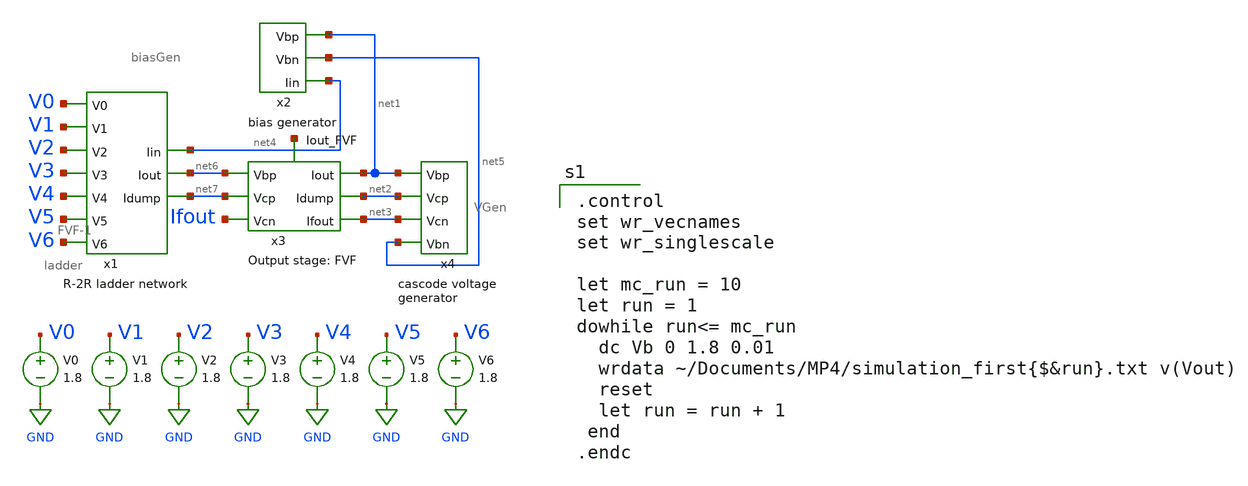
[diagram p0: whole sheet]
** sch_path: xschem/MP4-simulation-1.sch
**.subckt MP4-simulation-1
V1 V1 GND 1.8
V2 V2 GND 1.8
V3 V3 GND 1.8
V4 V4 GND 1.8
V5 V5 GND 1.8
V6 V6 GND 1.8
V0 V0 GND 1.8
x1 net4 net7 net6 V0 V1 V2 V3 V4 V5 V6 ladder
x2 net1 net4 net5 biasGen
x3 net6 net7 net1 Ifout net3 net2 net8 FVF-1
x4 net1 net3 net2 net5 VGen
**** begin user architecture code

.option wnflag=1
.param MC_SWITCH=0.0
.lib ~/skywater/skywater-pdk/libraries/sky130_fd_pr_ngspice/latest/models/sky130.lib.spice tt


.control
set wr_vecnames
set wr_singlescale

let mc_run = 10
let run = 1
dowhile run<= mc_run
  dc Vb 0 1.8 0.01
  wrdata ~/Documents/MP4/simulation_first{$&run}.txt v(Vout)
  reset
  let run = run + 1
 end
.endc

**** end user architecture code
**.ends

* expanding   symbol:  /home/madvlsi/DAC-VLSI/xschem/ladder.sym # of pins=10
** sym_path: /home/madvlsi/DAC-VLSI/xschem/ladder.sym
** sch_path: /home/madvlsi/DAC-VLSI/xschem/ladder.sch
.subckt ladder Iin Idump Iout V0 V1 V2 V3 V4 V5 V6
*.ipin Iin
*.ipin V0
*.ipin V1
*.ipin V2
*.ipin V3
*.ipin V4
*.ipin V5
*.ipin V6
*.opin Idump
*.opin Iout
XM1 Iin VDD net1 GND sky130_fd_pr__nfet_01v8 L=0.15 W=1 nf=1 ad='int((nf+1)/2) * W/nf * 0.29' as='int((nf+2)/2) * W/nf * 0.29'
+ pd='2*int((nf+1)/2) * (W/nf + 0.29)' ps='2*int((nf+2)/2) * (W/nf + 0.29)' nrd='0.29 / W' nrs='0.29 / W'
+ sa=0 sb=0 sd=0 mult=1 m=1
XM3 Iin VDD net3 GND sky130_fd_pr__nfet_01v8 L=0.15 W=1 nf=1 ad='int((nf+1)/2) * W/nf * 0.29' as='int((nf+2)/2) * W/nf * 0.29'
+ pd='2*int((nf+1)/2) * (W/nf + 0.29)' ps='2*int((nf+2)/2) * (W/nf + 0.29)' nrd='0.29 / W' nrs='0.29 / W'
+ sa=0 sb=0 sd=0 mult=1 m=1
XM5 net3 VDD net4 GND sky130_fd_pr__nfet_01v8 L=0.15 W=1 nf=1 ad='int((nf+1)/2) * W/nf * 0.29' as='int((nf+2)/2) * W/nf * 0.29'
+ pd='2*int((nf+1)/2) * (W/nf + 0.29)' ps='2*int((nf+2)/2) * (W/nf + 0.29)' nrd='0.29 / W' nrs='0.29 / W'
+ sa=0 sb=0 sd=0 mult=1 m=1
XM7 net3 VDD net6 GND sky130_fd_pr__nfet_01v8 L=0.15 W=1 nf=1 ad='int((nf+1)/2) * W/nf * 0.29' as='int((nf+2)/2) * W/nf * 0.29'
+ pd='2*int((nf+1)/2) * (W/nf + 0.29)' ps='2*int((nf+2)/2) * (W/nf + 0.29)' nrd='0.29 / W' nrs='0.29 / W'
+ sa=0 sb=0 sd=0 mult=1 m=1
XM6 net4 V1 net2 GND sky130_fd_pr__nfet_01v8 L=0.15 W=1 nf=1 ad='int((nf+1)/2) * W/nf * 0.29' as='int((nf+2)/2) * W/nf * 0.29'
+ pd='2*int((nf+1)/2) * (W/nf + 0.29)' ps='2*int((nf+2)/2) * (W/nf + 0.29)' nrd='0.29 / W' nrs='0.29 / W'
+ sa=0 sb=0 sd=0 mult=1 m=1
XM8 net4 net18 net5 GND sky130_fd_pr__nfet_01v8 L=0.15 W=1 nf=1 ad='int((nf+1)/2) * W/nf * 0.29' as='int((nf+2)/2) * W/nf * 0.29'
+ pd='2*int((nf+1)/2) * (W/nf + 0.29)' ps='2*int((nf+2)/2) * (W/nf + 0.29)' nrd='0.29 / W' nrs='0.29 / W'
+ sa=0 sb=0 sd=0 mult=1 m=1
XM2 net1 V0 net2 GND sky130_fd_pr__nfet_01v8 L=0.15 W=1 nf=1 ad='int((nf+1)/2) * W/nf * 0.29' as='int((nf+2)/2) * W/nf * 0.29'
+ pd='2*int((nf+1)/2) * (W/nf + 0.29)' ps='2*int((nf+2)/2) * (W/nf + 0.29)' nrd='0.29 / W' nrs='0.29 / W'
+ sa=0 sb=0 sd=0 mult=1 m=1
XM4 net1 net17 net5 GND sky130_fd_pr__nfet_01v8 L=0.15 W=1 nf=1 ad='int((nf+1)/2) * W/nf * 0.29' as='int((nf+2)/2) * W/nf * 0.29'
+ pd='2*int((nf+1)/2) * (W/nf + 0.29)' ps='2*int((nf+2)/2) * (W/nf + 0.29)' nrd='0.29 / W' nrs='0.29 / W'
+ sa=0 sb=0 sd=0 mult=1 m=1
XM9 net6 VDD net7 GND sky130_fd_pr__nfet_01v8 L=0.15 W=1 nf=1 ad='int((nf+1)/2) * W/nf * 0.29' as='int((nf+2)/2) * W/nf * 0.29'
+ pd='2*int((nf+1)/2) * (W/nf + 0.29)' ps='2*int((nf+2)/2) * (W/nf + 0.29)' nrd='0.29 / W' nrs='0.29 / W'
+ sa=0 sb=0 sd=0 mult=1 m=1
XM11 net6 VDD net8 GND sky130_fd_pr__nfet_01v8 L=0.15 W=1 nf=1 ad='int((nf+1)/2) * W/nf * 0.29' as='int((nf+2)/2) * W/nf * 0.29'
+ pd='2*int((nf+1)/2) * (W/nf + 0.29)' ps='2*int((nf+2)/2) * (W/nf + 0.29)' nrd='0.29 / W' nrs='0.29 / W'
+ sa=0 sb=0 sd=0 mult=1 m=1
XM10 net7 V2 net2 GND sky130_fd_pr__nfet_01v8 L=0.15 W=1 nf=1 ad='int((nf+1)/2) * W/nf * 0.29' as='int((nf+2)/2) * W/nf * 0.29'
+ pd='2*int((nf+1)/2) * (W/nf + 0.29)' ps='2*int((nf+2)/2) * (W/nf + 0.29)' nrd='0.29 / W' nrs='0.29 / W'
+ sa=0 sb=0 sd=0 mult=1 m=1
XM12 net7 net19 net5 GND sky130_fd_pr__nfet_01v8 L=0.15 W=1 nf=1 ad='int((nf+1)/2) * W/nf * 0.29' as='int((nf+2)/2) * W/nf * 0.29'
+ pd='2*int((nf+1)/2) * (W/nf + 0.29)' ps='2*int((nf+2)/2) * (W/nf + 0.29)' nrd='0.29 / W' nrs='0.29 / W'
+ sa=0 sb=0 sd=0 mult=1 m=1
XM13 net8 VDD net9 GND sky130_fd_pr__nfet_01v8 L=0.15 W=1 nf=1 ad='int((nf+1)/2) * W/nf * 0.29' as='int((nf+2)/2) * W/nf * 0.29'
+ pd='2*int((nf+1)/2) * (W/nf + 0.29)' ps='2*int((nf+2)/2) * (W/nf + 0.29)' nrd='0.29 / W' nrs='0.29 / W'
+ sa=0 sb=0 sd=0 mult=1 m=1
XM15 net8 VDD net10 GND sky130_fd_pr__nfet_01v8 L=0.15 W=1 nf=1 ad='int((nf+1)/2) * W/nf * 0.29' as='int((nf+2)/2) * W/nf * 0.29'
+ pd='2*int((nf+1)/2) * (W/nf + 0.29)' ps='2*int((nf+2)/2) * (W/nf + 0.29)' nrd='0.29 / W' nrs='0.29 / W'
+ sa=0 sb=0 sd=0 mult=1 m=1
XM14 net9 V3 net2 GND sky130_fd_pr__nfet_01v8 L=0.15 W=1 nf=1 ad='int((nf+1)/2) * W/nf * 0.29' as='int((nf+2)/2) * W/nf * 0.29'
+ pd='2*int((nf+1)/2) * (W/nf + 0.29)' ps='2*int((nf+2)/2) * (W/nf + 0.29)' nrd='0.29 / W' nrs='0.29 / W'
+ sa=0 sb=0 sd=0 mult=1 m=1
XM16 net9 net20 net5 GND sky130_fd_pr__nfet_01v8 L=0.15 W=1 nf=1 ad='int((nf+1)/2) * W/nf * 0.29' as='int((nf+2)/2) * W/nf * 0.29'
+ pd='2*int((nf+1)/2) * (W/nf + 0.29)' ps='2*int((nf+2)/2) * (W/nf + 0.29)' nrd='0.29 / W' nrs='0.29 / W'
+ sa=0 sb=0 sd=0 mult=1 m=1
XM17 net10 VDD net11 GND sky130_fd_pr__nfet_01v8 L=0.15 W=1 nf=1 ad='int((nf+1)/2) * W/nf * 0.29' as='int((nf+2)/2) * W/nf * 0.29'
+ pd='2*int((nf+1)/2) * (W/nf + 0.29)' ps='2*int((nf+2)/2) * (W/nf + 0.29)' nrd='0.29 / W' nrs='0.29 / W'
+ sa=0 sb=0 sd=0 mult=1 m=1
XM19 net10 VDD net12 GND sky130_fd_pr__nfet_01v8 L=0.15 W=1 nf=1 ad='int((nf+1)/2) * W/nf * 0.29' as='int((nf+2)/2) * W/nf * 0.29'
+ pd='2*int((nf+1)/2) * (W/nf + 0.29)' ps='2*int((nf+2)/2) * (W/nf + 0.29)' nrd='0.29 / W' nrs='0.29 / W'
+ sa=0 sb=0 sd=0 mult=1 m=1
XM18 net11 V4 net2 GND sky130_fd_pr__nfet_01v8 L=0.15 W=1 nf=1 ad='int((nf+1)/2) * W/nf * 0.29' as='int((nf+2)/2) * W/nf * 0.29'
+ pd='2*int((nf+1)/2) * (W/nf + 0.29)' ps='2*int((nf+2)/2) * (W/nf + 0.29)' nrd='0.29 / W' nrs='0.29 / W'
+ sa=0 sb=0 sd=0 mult=1 m=1
XM20 net11 net21 net5 GND sky130_fd_pr__nfet_01v8 L=0.15 W=1 nf=1 ad='int((nf+1)/2) * W/nf * 0.29' as='int((nf+2)/2) * W/nf * 0.29'
+ pd='2*int((nf+1)/2) * (W/nf + 0.29)' ps='2*int((nf+2)/2) * (W/nf + 0.29)' nrd='0.29 / W' nrs='0.29 / W'
+ sa=0 sb=0 sd=0 mult=1 m=1
XM21 net12 VDD net13 GND sky130_fd_pr__nfet_01v8 L=0.15 W=1 nf=1 ad='int((nf+1)/2) * W/nf * 0.29' as='int((nf+2)/2) * W/nf * 0.29'
+ pd='2*int((nf+1)/2) * (W/nf + 0.29)' ps='2*int((nf+2)/2) * (W/nf + 0.29)' nrd='0.29 / W' nrs='0.29 / W'
+ sa=0 sb=0 sd=0 mult=1 m=1
XM23 net12 VDD net14 GND sky130_fd_pr__nfet_01v8 L=0.15 W=1 nf=1 ad='int((nf+1)/2) * W/nf * 0.29' as='int((nf+2)/2) * W/nf * 0.29'
+ pd='2*int((nf+1)/2) * (W/nf + 0.29)' ps='2*int((nf+2)/2) * (W/nf + 0.29)' nrd='0.29 / W' nrs='0.29 / W'
+ sa=0 sb=0 sd=0 mult=1 m=1
XM22 net13 V5 net2 GND sky130_fd_pr__nfet_01v8 L=0.15 W=1 nf=1 ad='int((nf+1)/2) * W/nf * 0.29' as='int((nf+2)/2) * W/nf * 0.29'
+ pd='2*int((nf+1)/2) * (W/nf + 0.29)' ps='2*int((nf+2)/2) * (W/nf + 0.29)' nrd='0.29 / W' nrs='0.29 / W'
+ sa=0 sb=0 sd=0 mult=1 m=1
XM24 net13 net22 net5 GND sky130_fd_pr__nfet_01v8 L=0.15 W=1 nf=1 ad='int((nf+1)/2) * W/nf * 0.29' as='int((nf+2)/2) * W/nf * 0.29'
+ pd='2*int((nf+1)/2) * (W/nf + 0.29)' ps='2*int((nf+2)/2) * (W/nf + 0.29)' nrd='0.29 / W' nrs='0.29 / W'
+ sa=0 sb=0 sd=0 mult=1 m=1
XM25 net14 VDD net15 GND sky130_fd_pr__nfet_01v8 L=0.15 W=1 nf=1 ad='int((nf+1)/2) * W/nf * 0.29' as='int((nf+2)/2) * W/nf * 0.29'
+ pd='2*int((nf+1)/2) * (W/nf + 0.29)' ps='2*int((nf+2)/2) * (W/nf + 0.29)' nrd='0.29 / W' nrs='0.29 / W'
+ sa=0 sb=0 sd=0 mult=1 m=1
XM27 net14 VDD net16 GND sky130_fd_pr__nfet_01v8 L=0.15 W=1 nf=1 ad='int((nf+1)/2) * W/nf * 0.29' as='int((nf+2)/2) * W/nf * 0.29'
+ pd='2*int((nf+1)/2) * (W/nf + 0.29)' ps='2*int((nf+2)/2) * (W/nf + 0.29)' nrd='0.29 / W' nrs='0.29 / W'
+ sa=0 sb=0 sd=0 mult=1 m=1
XM26 net15 V6 net2 GND sky130_fd_pr__nfet_01v8 L=0.15 W=1 nf=1 ad='int((nf+1)/2) * W/nf * 0.29' as='int((nf+2)/2) * W/nf * 0.29'
+ pd='2*int((nf+1)/2) * (W/nf + 0.29)' ps='2*int((nf+2)/2) * (W/nf + 0.29)' nrd='0.29 / W' nrs='0.29 / W'
+ sa=0 sb=0 sd=0 mult=1 m=1
XM28 net15 net23 net5 GND sky130_fd_pr__nfet_01v8 L=0.15 W=1 nf=1 ad='int((nf+1)/2) * W/nf * 0.29' as='int((nf+2)/2) * W/nf * 0.29'
+ pd='2*int((nf+1)/2) * (W/nf + 0.29)' ps='2*int((nf+2)/2) * (W/nf + 0.29)' nrd='0.29 / W' nrs='0.29 / W'
+ sa=0 sb=0 sd=0 mult=1 m=1
XM29 net16 VDD net5 GND sky130_fd_pr__nfet_01v8 L=0.15 W=1 nf=1 ad='int((nf+1)/2) * W/nf * 0.29' as='int((nf+2)/2) * W/nf * 0.29'
+ pd='2*int((nf+1)/2) * (W/nf + 0.29)' ps='2*int((nf+2)/2) * (W/nf + 0.29)' nrd='0.29 / W' nrs='0.29 / W'
+ sa=0 sb=0 sd=0 mult=1 m=1
XM30 GND net5 net5 GND sky130_fd_pr__nfet_01v8 L=0.15 W=1 nf=1 ad='int((nf+1)/2) * W/nf * 0.29' as='int((nf+2)/2) * W/nf * 0.29'
+ pd='2*int((nf+1)/2) * (W/nf + 0.29)' ps='2*int((nf+2)/2) * (W/nf + 0.29)' nrd='0.29 / W' nrs='0.29 / W'
+ sa=0 sb=0 sd=0 mult=1 m=1
XM31 GND net2 net2 GND sky130_fd_pr__nfet_01v8 L=0.15 W=1 nf=1 ad='int((nf+1)/2) * W/nf * 0.29' as='int((nf+2)/2) * W/nf * 0.29'
+ pd='2*int((nf+1)/2) * (W/nf + 0.29)' ps='2*int((nf+2)/2) * (W/nf + 0.29)' nrd='0.29 / W' nrs='0.29 / W'
+ sa=0 sb=0 sd=0 mult=1 m=1
XM32 Idump net5 GND GND sky130_fd_pr__nfet_01v8 L=0.15 W=1 nf=1 ad='int((nf+1)/2) * W/nf * 0.29' as='int((nf+2)/2) * W/nf * 0.29'
+ pd='2*int((nf+1)/2) * (W/nf + 0.29)' ps='2*int((nf+2)/2) * (W/nf + 0.29)' nrd='0.29 / W' nrs='0.29 / W'
+ sa=0 sb=0 sd=0 mult=1 m=1
XM33 Iout net2 GND GND sky130_fd_pr__nfet_01v8 L=0.15 W=1 nf=1 ad='int((nf+1)/2) * W/nf * 0.29' as='int((nf+2)/2) * W/nf * 0.29'
+ pd='2*int((nf+1)/2) * (W/nf + 0.29)' ps='2*int((nf+2)/2) * (W/nf + 0.29)' nrd='0.29 / W' nrs='0.29 / W'
+ sa=0 sb=0 sd=0 mult=1 m=1
x1 net17 V0 inverter
x2 net18 V1 inverter
x3 net19 V2 inverter
x4 net20 V3 inverter
x5 net21 V4 inverter
x6 net22 V5 inverter
x7 net23 V6 inverter
.ends


* expanding   symbol:  /home/madvlsi/DAC-VLSI/xschem/biasGen.sym # of pins=3
** sym_path: xschem/biasGen.sym
** sch_path: xschem/biasGen.sch
.subckt biasGen Vbp Iin Vbn
*.opin Iin
*.opin Vbp
*.opin Vbn
XM1 Vbn Vbn GND GND sky130_fd_pr__nfet_01v8 L=0.15 W=1 nf=1 ad='int((nf+1)/2) * W/nf * 0.29' as='int((nf+2)/2) * W/nf * 0.29'
+ pd='2*int((nf+1)/2) * (W/nf + 0.29)' ps='2*int((nf+2)/2) * (W/nf + 0.29)' nrd='0.29 / W' nrs='0.29 / W'
+ sa=0 sb=0 sd=0 mult=1 m=1
XM2 GND Vbn Vbp GND sky130_fd_pr__nfet_01v8 L=0.15 W=1 nf=1 ad='int((nf+1)/2) * W/nf * 0.29' as='int((nf+2)/2) * W/nf * 0.29'
+ pd='2*int((nf+1)/2) * (W/nf + 0.29)' ps='2*int((nf+2)/2) * (W/nf + 0.29)' nrd='0.29 / W' nrs='0.29 / W'
+ sa=0 sb=0 sd=0 mult=1 m=1
XM3 net1 net2 GND GND sky130_fd_pr__nfet_01v8 L=0.15 W=1 nf=1 ad='int((nf+1)/2) * W/nf * 0.29' as='int((nf+2)/2) * W/nf * 0.29'
+ pd='2*int((nf+1)/2) * (W/nf + 0.29)' ps='2*int((nf+2)/2) * (W/nf + 0.29)' nrd='0.29 / W' nrs='0.29 / W'
+ sa=0 sb=0 sd=0 mult=1 m=1
XM4 net3 net2 net2 GND sky130_fd_pr__nfet_01v8 L=0.15 W=8 nf=1 ad='int((nf+1)/2) * W/nf * 0.29' as='int((nf+2)/2) * W/nf * 0.29'
+ pd='2*int((nf+1)/2) * (W/nf + 0.29)' ps='2*int((nf+2)/2) * (W/nf + 0.29)' nrd='0.29 / W' nrs='0.29 / W'
+ sa=0 sb=0 sd=0 mult=1 m=1
XM5 Vbp net1 VDD VDD sky130_fd_pr__pfet_01v8 L=0.15 W=1 nf=1 ad='int((nf+1)/2) * W/nf * 0.29' as='int((nf+2)/2) * W/nf * 0.29'
+ pd='2*int((nf+1)/2) * (W/nf + 0.29)' ps='2*int((nf+2)/2) * (W/nf + 0.29)' nrd='0.29 / W' nrs='0.29 / W'
+ sa=0 sb=0 sd=0 mult=1 m=1
XM6 VDD net1 net1 VDD sky130_fd_pr__pfet_01v8 L=0.15 W=1 nf=1 ad='int((nf+1)/2) * W/nf * 0.29' as='int((nf+2)/2) * W/nf * 0.29'
+ pd='2*int((nf+1)/2) * (W/nf + 0.29)' ps='2*int((nf+2)/2) * (W/nf + 0.29)' nrd='0.29 / W' nrs='0.29 / W'
+ sa=0 sb=0 sd=0 mult=1 m=1
XM7 VDD Vbp net2 VDD sky130_fd_pr__pfet_01v8 L=0.15 W=1 nf=1 ad='int((nf+1)/2) * W/nf * 0.29' as='int((nf+2)/2) * W/nf * 0.29'
+ pd='2*int((nf+1)/2) * (W/nf + 0.29)' ps='2*int((nf+2)/2) * (W/nf + 0.29)' nrd='0.29 / W' nrs='0.29 / W'
+ sa=0 sb=0 sd=0 mult=1 m=1
XM8 Vbn Vbp VDD VDD sky130_fd_pr__pfet_01v8 L=0.15 W=1 nf=1 ad='int((nf+1)/2) * W/nf * 0.29' as='int((nf+2)/2) * W/nf * 0.29'
+ pd='2*int((nf+1)/2) * (W/nf + 0.29)' ps='2*int((nf+2)/2) * (W/nf + 0.29)' nrd='0.29 / W' nrs='0.29 / W'
+ sa=0 sb=0 sd=0 mult=1 m=1
R1 net3 GND 100k m=1
XM9 Iin Vbp VDD VDD sky130_fd_pr__pfet_01v8 L=0.15 W=1 nf=1 ad='int((nf+1)/2) * W/nf * 0.29' as='int((nf+2)/2) * W/nf * 0.29'
+ pd='2*int((nf+1)/2) * (W/nf + 0.29)' ps='2*int((nf+2)/2) * (W/nf + 0.29)' nrd='0.29 / W' nrs='0.29 / W'
+ sa=0 sb=0 sd=0 mult=1 m=1
.ends


* expanding   symbol:  /home/madvlsi/DAC-VLSI/xschem/FVF-1.sym # of pins=7
** sym_path: xschem/old_files/FVF-1.sym
** sch_path: xschem/old_files/FVF-1.sch
.subckt FVF-1 Vbp Vcp Iout Vcn Ifout Idump Iout_FVF
*.ipin Vcn
*.ipin Iout
*.ipin Idump
*.ipin Vcp
*.ipin Vbp
*.opin Ifout
*.opin Iout_FVF
XM1 net1 Vcn Idump GND sky130_fd_pr__nfet_01v8 L=8 W=24 nf=1 ad='int((nf+1)/2) * W/nf * 0.29' as='int((nf+2)/2) * W/nf * 0.29'
+ pd='2*int((nf+1)/2) * (W/nf + 0.29)' ps='2*int((nf+2)/2) * (W/nf + 0.29)' nrd='0.29 / W' nrs='0.29 / W'
+ sa=0 sb=0 sd=0 mult=1 m=1
XM2 GND net1 Idump GND sky130_fd_pr__nfet_01v8 L=8 W=24 nf=1 ad='int((nf+1)/2) * W/nf * 0.29' as='int((nf+2)/2) * W/nf * 0.29'
+ pd='2*int((nf+1)/2) * (W/nf + 0.29)' ps='2*int((nf+2)/2) * (W/nf + 0.29)' nrd='0.29 / W' nrs='0.29 / W'
+ sa=0 sb=0 sd=0 mult=1 m=1
XM3 Iout_FVF Vcn Iout GND sky130_fd_pr__nfet_01v8 L=8 W=24 nf=1 ad='int((nf+1)/2) * W/nf * 0.29' as='int((nf+2)/2) * W/nf * 0.29'
+ pd='2*int((nf+1)/2) * (W/nf + 0.29)' ps='2*int((nf+2)/2) * (W/nf + 0.29)' nrd='0.29 / W' nrs='0.29 / W'
+ sa=0 sb=0 sd=0 mult=1 m=1
XM4 GND Iout_FVF Iout GND sky130_fd_pr__nfet_01v8 L=8 W=24 nf=1 ad='int((nf+1)/2) * W/nf * 0.29' as='int((nf+2)/2) * W/nf * 0.29'
+ pd='2*int((nf+1)/2) * (W/nf + 0.29)' ps='2*int((nf+2)/2) * (W/nf + 0.29)' nrd='0.29 / W' nrs='0.29 / W'
+ sa=0 sb=0 sd=0 mult=1 m=1
XM5 Ifout Vcn net2 GND sky130_fd_pr__nfet_01v8 L=8 W=24 nf=1 ad='int((nf+1)/2) * W/nf * 0.29' as='int((nf+2)/2) * W/nf * 0.29'
+ pd='2*int((nf+1)/2) * (W/nf + 0.29)' ps='2*int((nf+2)/2) * (W/nf + 0.29)' nrd='0.29 / W' nrs='0.29 / W'
+ sa=0 sb=0 sd=0 mult=1 m=1
XM6 net2 Iout_FVF GND GND sky130_fd_pr__nfet_01v8 L=8 W=24 nf=1 ad='int((nf+1)/2) * W/nf * 0.29' as='int((nf+2)/2) * W/nf * 0.29'
+ pd='2*int((nf+1)/2) * (W/nf + 0.29)' ps='2*int((nf+2)/2) * (W/nf + 0.29)' nrd='0.29 / W' nrs='0.29 / W'
+ sa=0 sb=0 sd=0 mult=1 m=1
XM7 net1 Vcp net3 VDD sky130_fd_pr__pfet_01v8 L=8 W=24 nf=1 ad='int((nf+1)/2) * W/nf * 0.29' as='int((nf+2)/2) * W/nf * 0.29'
+ pd='2*int((nf+1)/2) * (W/nf + 0.29)' ps='2*int((nf+2)/2) * (W/nf + 0.29)' nrd='0.29 / W' nrs='0.29 / W'
+ sa=0 sb=0 sd=0 mult=1 m=1
XM8 Iout_FVF Vcp net4 VDD sky130_fd_pr__pfet_01v8 L=8 W=24 nf=1 ad='int((nf+1)/2) * W/nf * 0.29' as='int((nf+2)/2) * W/nf * 0.29'
+ pd='2*int((nf+1)/2) * (W/nf + 0.29)' ps='2*int((nf+2)/2) * (W/nf + 0.29)' nrd='0.29 / W' nrs='0.29 / W'
+ sa=0 sb=0 sd=0 mult=1 m=1
XM9 Ifout Vcp net5 VDD sky130_fd_pr__pfet_01v8 L=8 W=24 nf=1 ad='int((nf+1)/2) * W/nf * 0.29' as='int((nf+2)/2) * W/nf * 0.29'
+ pd='2*int((nf+1)/2) * (W/nf + 0.29)' ps='2*int((nf+2)/2) * (W/nf + 0.29)' nrd='0.29 / W' nrs='0.29 / W'
+ sa=0 sb=0 sd=0 mult=1 m=1
XM15 net3 Vbp VDD VDD sky130_fd_pr__pfet_01v8 L=8 W=24 nf=1 ad='int((nf+1)/2) * W/nf * 0.29' as='int((nf+2)/2) * W/nf * 0.29'
+ pd='2*int((nf+1)/2) * (W/nf + 0.29)' ps='2*int((nf+2)/2) * (W/nf + 0.29)' nrd='0.29 / W' nrs='0.29 / W'
+ sa=0 sb=0 sd=0 mult=1 m=1
XM16 net4 Vbp VDD VDD sky130_fd_pr__pfet_01v8 L=8 W=24 nf=1 ad='int((nf+1)/2) * W/nf * 0.29' as='int((nf+2)/2) * W/nf * 0.29'
+ pd='2*int((nf+1)/2) * (W/nf + 0.29)' ps='2*int((nf+2)/2) * (W/nf + 0.29)' nrd='0.29 / W' nrs='0.29 / W'
+ sa=0 sb=0 sd=0 mult=1 m=1
XM17 net5 Vbp VDD VDD sky130_fd_pr__pfet_01v8 L=8 W=24 nf=1 ad='int((nf+1)/2) * W/nf * 0.29' as='int((nf+2)/2) * W/nf * 0.29'
+ pd='2*int((nf+1)/2) * (W/nf + 0.29)' ps='2*int((nf+2)/2) * (W/nf + 0.29)' nrd='0.29 / W' nrs='0.29 / W'
+ sa=0 sb=0 sd=0 mult=1 m=1
.ends


* expanding   symbol:  /home/madvlsi/DAC-VLSI/xschem/VGen.sym # of pins=4
** sym_path: xschem/VGen.sym
** sch_path: xschem/VGen.sch
.subckt VGen Vbp Vcn Vcp Vbn
*.opin Vcp
*.ipin Vbp
*.ipin Vbn
*.opin Vcn
XM5 net4 net4 net1 GND sky130_fd_pr__nfet_01v8 L=0.5 W=24 nf=1 ad='int((nf+1)/2) * W/nf * 0.29' as='int((nf+2)/2) * W/nf * 0.29'
+ pd='2*int((nf+1)/2) * (W/nf + 0.29)' ps='2*int((nf+2)/2) * (W/nf + 0.29)' nrd='0.29 / W' nrs='0.29 / W'
+ sa=0 sb=0 sd=0 mult=1 m=1
XM6 net1 net4 GND GND sky130_fd_pr__nfet_01v8 L=0.5 W=12 nf=1 ad='int((nf+1)/2) * W/nf * 0.29' as='int((nf+2)/2) * W/nf * 0.29'
+ pd='2*int((nf+1)/2) * (W/nf + 0.29)' ps='2*int((nf+2)/2) * (W/nf + 0.29)' nrd='0.29 / W' nrs='0.29 / W'
+ sa=0 sb=0 sd=0 mult=1 m=1
XM4 net1 Vcn Vcn GND sky130_fd_pr__nfet_01v8 L=0.5 W=12 nf=1 ad='int((nf+1)/2) * W/nf * 0.29' as='int((nf+2)/2) * W/nf * 0.29'
+ pd='2*int((nf+1)/2) * (W/nf + 0.29)' ps='2*int((nf+2)/2) * (W/nf + 0.29)' nrd='0.29 / W' nrs='0.29 / W'
+ sa=0 sb=0 sd=0 mult=1 m=1
XM1 VDD Vbp net4 VDD sky130_fd_pr__pfet_01v8 L=0.5 W=6 nf=1 ad='int((nf+1)/2) * W/nf * 0.29' as='int((nf+2)/2) * W/nf * 0.29'
+ pd='2*int((nf+1)/2) * (W/nf + 0.29)' ps='2*int((nf+2)/2) * (W/nf + 0.29)' nrd='0.29 / W' nrs='0.29 / W'
+ sa=0 sb=0 sd=0 mult=1 m=1
XM2 VDD Vbp Vcn VDD sky130_fd_pr__pfet_01v8 L=0.5 W=12 nf=1 ad='int((nf+1)/2) * W/nf * 0.29' as='int((nf+2)/2) * W/nf * 0.29'
+ pd='2*int((nf+1)/2) * (W/nf + 0.29)' ps='2*int((nf+2)/2) * (W/nf + 0.29)' nrd='0.29 / W' nrs='0.29 / W'
+ sa=0 sb=0 sd=0 mult=1 m=1
XM9 net3 net3 net2 VDD sky130_fd_pr__pfet_01v8 L=0.5 W=24 nf=1 ad='int((nf+1)/2) * W/nf * 0.29' as='int((nf+2)/2) * W/nf * 0.29'
+ pd='2*int((nf+1)/2) * (W/nf + 0.29)' ps='2*int((nf+2)/2) * (W/nf + 0.29)' nrd='0.29 / W' nrs='0.29 / W'
+ sa=0 sb=0 sd=0 mult=1 m=1
XM11 GND Vbn Vcp GND sky130_fd_pr__nfet_01v8 L=0.5 W=12 nf=1 ad='int((nf+1)/2) * W/nf * 0.29' as='int((nf+2)/2) * W/nf * 0.29'
+ pd='2*int((nf+1)/2) * (W/nf + 0.29)' ps='2*int((nf+2)/2) * (W/nf + 0.29)' nrd='0.29 / W' nrs='0.29 / W'
+ sa=0 sb=0 sd=0 mult=1 m=1
XM8 net2 Vcp Vcp VDD sky130_fd_pr__pfet_01v8 L=0.5 W=12 nf=1 ad='int((nf+1)/2) * W/nf * 0.29' as='int((nf+2)/2) * W/nf * 0.29'
+ pd='2*int((nf+1)/2) * (W/nf + 0.29)' ps='2*int((nf+2)/2) * (W/nf + 0.29)' nrd='0.29 / W' nrs='0.29 / W'
+ sa=0 sb=0 sd=0 mult=1 m=1
XM12 GND Vbn net3 GND sky130_fd_pr__nfet_01v8 L=0.5 W=6 nf=1 ad='int((nf+1)/2) * W/nf * 0.29' as='int((nf+2)/2) * W/nf * 0.29'
+ pd='2*int((nf+1)/2) * (W/nf + 0.29)' ps='2*int((nf+2)/2) * (W/nf + 0.29)' nrd='0.29 / W' nrs='0.29 / W'
+ sa=0 sb=0 sd=0 mult=1 m=1
XM7 net2 net3 VDD VDD sky130_fd_pr__pfet_01v8 L=0.5 W=12 nf=1 ad='int((nf+1)/2) * W/nf * 0.29' as='int((nf+2)/2) * W/nf * 0.29'
+ pd='2*int((nf+1)/2) * (W/nf + 0.29)' ps='2*int((nf+2)/2) * (W/nf + 0.29)' nrd='0.29 / W' nrs='0.29 / W'
+ sa=0 sb=0 sd=0 mult=1 m=1
.ends


* expanding   symbol:  ./inverter.sym # of pins=2
** sym_path: xschem/inverter.sym
** sch_path: xschem/inverter.sch
.subckt inverter Y A
*.ipin A
*.opin Y
XM1 Y A VDD VDD sky130_fd_pr__pfet_01v8 L=0.15 W=1 nf=1 ad='int((nf+1)/2) * W/nf * 0.29' as='int((nf+2)/2) * W/nf * 0.29'
+ pd='2*int((nf+1)/2) * (W/nf + 0.29)' ps='2*int((nf+2)/2) * (W/nf + 0.29)' nrd='0.29 / W' nrs='0.29 / W'
+ sa=0 sb=0 sd=0 mult=1 m=1
XM2 Y A GND GND sky130_fd_pr__nfet_01v8 L=0.15 W=1 nf=1 ad='int((nf+1)/2) * W/nf * 0.29' as='int((nf+2)/2) * W/nf * 0.29'
+ pd='2*int((nf+1)/2) * (W/nf + 0.29)' ps='2*int((nf+2)/2) * (W/nf + 0.29)' nrd='0.29 / W' nrs='0.29 / W'
+ sa=0 sb=0 sd=0 mult=1 m=1
.ends

.GLOBAL GND
.GLOBAL VDD
.end
